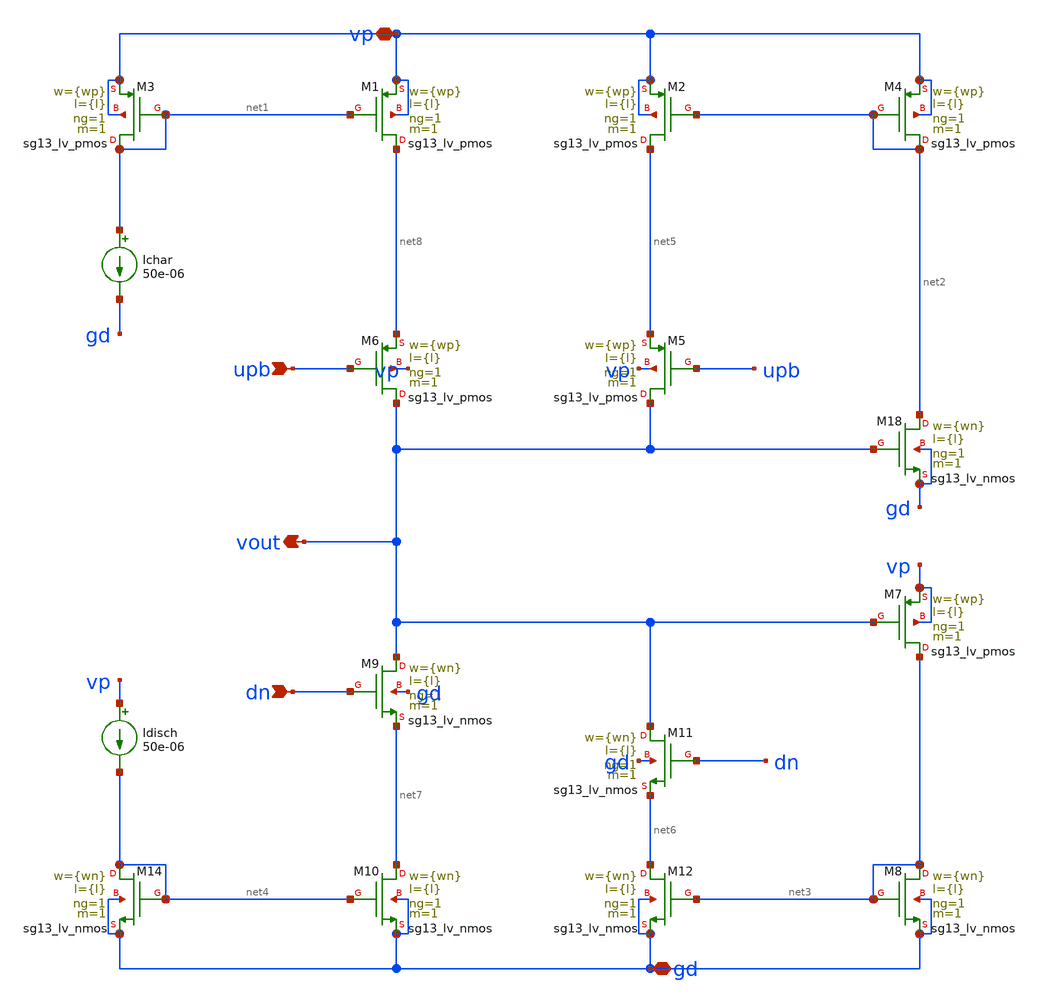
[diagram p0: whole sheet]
** sch_path: charge_pump/cp_v2.sch
**.subckt cp_v2 vp upb vout dn gd
*.iopin vp
*.ipin upb
*.opin vout
*.ipin dn
*.iopin gd
XM3 net1 net1 vp vp sg13_lv_pmos w={wp} l={l} ng=1 m=1 mm_ok=1
XM1 net8 net1 vp vp sg13_lv_pmos w={wp} l={l} ng=1 m=1 mm_ok=1
XM2 net5 net2 vp vp sg13_lv_pmos w={wp} l={l} ng=1 m=1 mm_ok=1
XM4 net2 net2 vp vp sg13_lv_pmos w={wp} l={l} ng=1 m=1 mm_ok=1
XM5 vout upb net5 vp sg13_lv_pmos w={wp} l={l} ng=1 m=1 mm_ok=1
XM6 vout upb net8 vp sg13_lv_pmos w={wp} l={l} ng=1 m=1 mm_ok=1
XM18 net2 vout gd gd sg13_lv_nmos w={wn} l={l} ng=1 m=1 mm_ok=1
XM7 net3 vout vp vp sg13_lv_pmos w={wp} l={l} ng=1 m=1 mm_ok=1
XM8 net3 net3 gd gd sg13_lv_nmos w={wn} l={l} ng=1 m=1 mm_ok=1
XM9 vout dn net7 gd sg13_lv_nmos w={wn} l={l} ng=1 m=1 mm_ok=1
XM10 net7 net4 gd gd sg13_lv_nmos w={wn} l={l} ng=1 m=1 mm_ok=1
XM11 vout dn net6 gd sg13_lv_nmos w={wn} l={l} ng=1 m=1 mm_ok=1
XM12 net6 net3 gd gd sg13_lv_nmos w={wn} l={l} ng=1 m=1 mm_ok=1
XM14 net4 net4 gd gd sg13_lv_nmos w={wn} l={l} ng=1 m=1 mm_ok=1
Ichar net1 gd 50e-06
Idisch vp net4 50e-06
**.ends
.end
